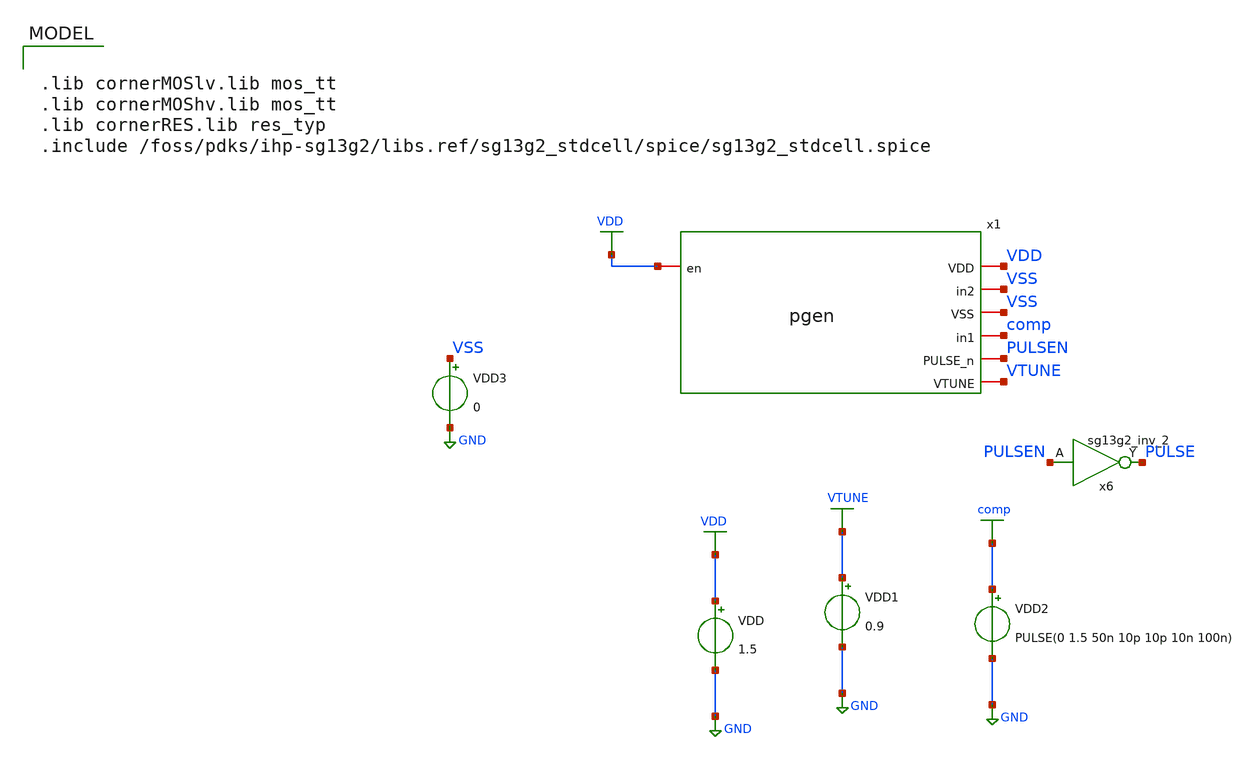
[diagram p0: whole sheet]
** sch_path: xschem/comparator/pulse_gen/testbench/tb_pgen.sch
* IHP-GmbH/IHP-Open-PDK/ihp-sg13g2/libs.tech/xschem/sg13g2_stdcells/sg13g2_inv_2.sch:
* Copyright 2023 IHP PDK Authors
* Licensed under the Apache License, Version 2.0 (the "License");
**.subckt tb_pgen
x1 VDD VSS VSS comp PULSEN VTUNE VDD pgen
VDD VDD GND 1.5
VDD1 VTUNE GND 0.9
VDD2 comp GND PULSE(0 1.5 50n 10p 10p 10n 100n)
x6 PULSE PULSEN VDD VSS sg13g2_inv_2
VDD3 VSS GND 0
**** begin user architecture code

.lib cornerMOSlv.lib mos_tt
.lib cornerMOShv.lib mos_tt
.lib cornerRES.lib res_typ
.include /foss/pdks/ihp-sg13g2/libs.ref/sg13g2_stdcell/spice/sg13g2_stdcell.spice



.param temp=27
*.options savecurrents reltol=1e-3 abstol=1e-12 gmin=1e-15
.control
save all

tran 4p 70n

* Plotting
plot v(comp) {v(x1.vx) + 2} {v(PULSE)  +4} {x1.READY + 6} {v(PULSEN) + 8} {x1.vx_n+10} {x1.vxs+12} {x1.vy+14}
+ {x1.vsti+16}

.endc

**** end user architecture code
**.ends

* expanding   symbol:  comparator/pulse_gen/pgen.sym # of pins=7
** sym_path: xschem/comparator/pulse_gen/pgen.sym
** sch_path: xschem/comparator/pulse_gen/pgen.sch
.subckt pgen VDD in2 VSS in1 PULSE_n VTUNE en
*.iopin VDD
*.iopin in2
*.iopin in1
*.iopin VSS
*.iopin VTUNE
*.iopin PULSE_n
*.iopin en
XM1 READY in1 VSS VSS sg13_lv_nmos w=1u l=0.13u ng=1 m=1 mm_ok=1
XM2 READY vx_n VDD VDD sg13_lv_pmos w=2u l=0.13u ng=1 m=1 mm_ok=1
XM4 vx vy net3 VDD sg13_lv_pmos w=2u l=0.13u ng=1 m=1 mm_ok=1
x46 vy vxs READY VDD VSS sg13g2_or2_2
x6 vx_n vxs VDD VSS sg13g2_inv_2
XM3 READY in2 VSS VSS sg13_lv_nmos w=1u l=0.13u ng=1 m=1 mm_ok=1
XM5 vx READY VSS VSS sg13_lv_nmos w=1u l=0.13u ng=1 m=1 mm_ok=1
XM7 net3 VTUNE VDD VDD sg13_lv_pmos w=2u l=0.5u ng=1 m=1 mm_ok=1
XM6 net2 vx VDD VDD sg13_lv_pmos w=0.15u l=0.13u ng=1 m=1 mm_ok=1
XM8 vsti vx net1 VSS sg13_lv_nmos w=0.15u l=0.13u ng=1 m=1 mm_ok=1
XM9 vsti vx net2 VDD sg13_lv_pmos w=0.15u l=0.13u ng=1 m=1 mm_ok=1
XM10 net1 vx VSS VSS sg13_lv_nmos w=0.15u l=0.13u ng=1 m=1 mm_ok=1
XM11 VDD vsti net1 VDD sg13_lv_nmos w=0.15u l=0.13u ng=1 m=1 mm_ok=1
XM12 VSS vsti net2 VSS sg13_lv_pmos w=0.15u l=0.13u ng=1 m=1 mm_ok=1
x1 vxs vsti VDD VSS sg13g2_inv_2
x2 PULSE_n vy en VDD VSS sg13g2_and2_2
XM14 READY en VDD VDD sg13_lv_pmos w=2u l=0.13u ng=1 m=1 mm_ok=1
.ends


* expanding   symbol:  sg13g2_stdcells/sg13g2_inv_2.sym # of pins=2
** sym_path: sg13g2_stdcells/sg13g2_inv_2.sym
** sch_path: sg13g2_stdcells/sg13g2_inv_2.sch
.subckt sg13g2_inv_2 Y A VDD VSS
*.opin Y
*.ipin A
*.iopin VDD
*.iopin VSS
XM1 Y A VSS VSS sg13_lv_nmos w=1.48u l=130.00n ng=2 m=1 mm_ok=1
XM2 Y A VDD VDD sg13_lv_pmos w=2.24u l=130.00n ng=2 m=1 mm_ok=1
.ends


* expanding   symbol:  sg13g2_stdcells/sg13g2_or2_2.sym # of pins=3
** sym_path: sg13g2_stdcells/sg13g2_or2_2.sym
** sch_path: sg13g2_stdcells/sg13g2_or2_2.sch
.subckt sg13g2_or2_2 X A B VDD VSS
*.opin X
*.ipin B
*.ipin A
*.iopin VDD
*.iopin VSS
XM1 net1 B VSS VSS sg13_lv_nmos w=550.00n l=130.00n ng=1 m=1 mm_ok=1
XM2 net1 A VSS VSS sg13_lv_nmos w=550.00n l=130.00n ng=1 m=1 mm_ok=1
XM3 X net1 VSS VSS sg13_lv_nmos w=1.48u l=130.00n ng=2 m=1 mm_ok=1
XM4 net2 A VDD VDD sg13_lv_pmos w=840.00n l=130.00n ng=1 m=1 mm_ok=1
XM5 net1 B net2 VDD sg13_lv_pmos w=840.00n l=130.00n ng=1 m=1 mm_ok=1
XM6 X net1 VDD VDD sg13_lv_pmos w=2.24u l=130.00n ng=2 m=1 mm_ok=1
.ends


* expanding   symbol:  sg13g2_stdcells/sg13g2_and2_2.sym # of pins=3
** sym_path: sg13g2_stdcells/sg13g2_and2_2.sym
** sch_path: sg13g2_stdcells/sg13g2_and2_2.sch
.subckt sg13g2_and2_2 X A B VDD VSS
*.ipin A
*.ipin B
*.opin X
*.iopin VDD
*.iopin VSS
XM1 net1 A net2 VSS sg13_lv_nmos w=640.00n l=130.00n ng=1 m=1 mm_ok=1
XM2 net2 B VSS VSS sg13_lv_nmos w=640.00n l=130.00n ng=1 m=1 mm_ok=1
XM3 X net1 VSS VSS sg13_lv_nmos w=1.48u l=130.00n ng=2 m=1 mm_ok=1
XM4 net1 B VDD VDD sg13_lv_pmos w=840.00n l=130.00n ng=1 m=1 mm_ok=1
XM5 net1 A VDD VDD sg13_lv_pmos w=840.00n l=130.00n ng=1 m=1 mm_ok=1
XM6 X net1 VDD VDD sg13_lv_pmos w=2.24u l=130.00n ng=2 m=1 mm_ok=1
.ends

.GLOBAL GND
.GLOBAL VDD
.GLOBAL VTUNE
.GLOBAL comp
.end
